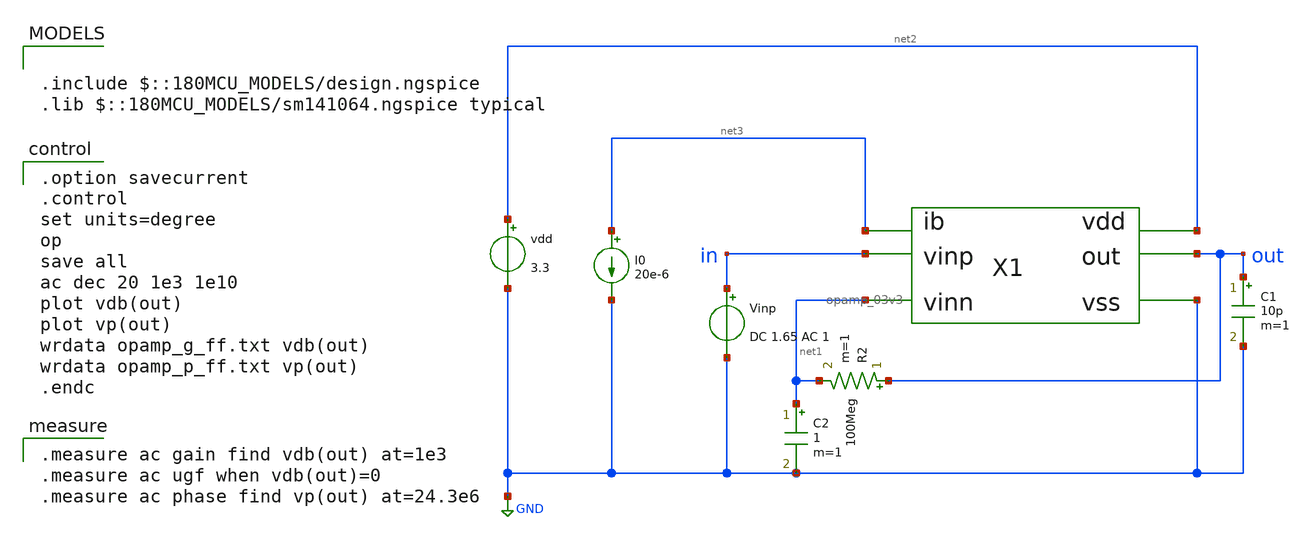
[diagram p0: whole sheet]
** sch_path: opamp_ac_03v3.sch
**.subckt opamp_ac_03v3
vdd net2 GND 3.3
I0 net3 GND 20e-6
Vinp in GND DC 1.65 AC 1
R2 out net1 100Meg m=1
C2 net1 GND 1 m=1
C1 out GND 10p m=1
X1 net1 in net3 GND out net2 opamp_03v3
**** begin user architecture code

.include $::180MCU_MODELS/design.ngspice
.lib $::180MCU_MODELS/sm141064.ngspice typical


.option savecurrent
.control
set units=degree
op
save all
ac dec 20 1e3 1e10
plot vdb(out)
plot vp(out)
wrdata opamp_g_ff.txt vdb(out)
wrdata opamp_p_ff.txt vp(out)
.endc


.measure ac gain find vdb(out) at=1e3
.measure ac ugf when vdb(out)=0
.measure ac phase find vp(out) at=24.3e6

**** end user architecture code
**.ends

* expanding   symbol:  opamp_03v3.sym # of pins=6
** sym_path: opamp_03v3.sym
** sch_path: opamp_03v3.sch
.subckt opamp_03v3 vinn vinp ib vss out vdd
*.iopin ib
*.iopin vdd
*.ipin vinn
*.opin out
*.iopin vss
*.ipin vinp
XM1 net4 vinn net3 net3 pfet_03v3 L=0.56u W=56u nf=1 ad='int((nf+1)/2) * W/nf * 0.18u' as='int((nf+2)/2) * W/nf * 0.18u'
+ pd='2*int((nf+1)/2) * (W/nf + 0.18u)' ps='2*int((nf+2)/2) * (W/nf + 0.18u)' nrd='0.18u / W' nrs='0.18u / W'
+ sa=0 sb=0 sd=0 m=1
XM2 net5 vinp net3 net3 pfet_03v3 L=0.56u W=56u nf=1 ad='int((nf+1)/2) * W/nf * 0.18u' as='int((nf+2)/2) * W/nf * 0.18u'
+ pd='2*int((nf+1)/2) * (W/nf + 0.18u)' ps='2*int((nf+2)/2) * (W/nf + 0.18u)' nrd='0.18u / W' nrs='0.18u / W'
+ sa=0 sb=0 sd=0 m=1
XM3 net4 net4 vss vss nfet_03v3 L=0.56u W=2.8u nf=1 ad='int((nf+1)/2) * W/nf * 0.18u' as='int((nf+2)/2) * W/nf * 0.18u'
+ pd='2*int((nf+1)/2) * (W/nf + 0.18u)' ps='2*int((nf+2)/2) * (W/nf + 0.18u)' nrd='0.18u / W' nrs='0.18u / W'
+ sa=0 sb=0 sd=0 m=1
XM4 net5 net4 vss vss nfet_03v3 L=0.56u W=2.8u nf=1 ad='int((nf+1)/2) * W/nf * 0.18u' as='int((nf+2)/2) * W/nf * 0.18u'
+ pd='2*int((nf+1)/2) * (W/nf + 0.18u)' ps='2*int((nf+2)/2) * (W/nf + 0.18u)' nrd='0.18u / W' nrs='0.18u / W'
+ sa=0 sb=0 sd=0 m=1
XM5 net3 ib vdd vdd pfet_03v3 L=0.56u W=11.2u nf=1 ad='int((nf+1)/2) * W/nf * 0.18u' as='int((nf+2)/2) * W/nf * 0.18u'
+ pd='2*int((nf+1)/2) * (W/nf + 0.18u)' ps='2*int((nf+2)/2) * (W/nf + 0.18u)' nrd='0.18u / W' nrs='0.18u / W'
+ sa=0 sb=0 sd=0 m=1
XM6 out ib vdd vdd pfet_03v3 L=0.56u W=56u nf=1 ad='int((nf+1)/2) * W/nf * 0.18u' as='int((nf+2)/2) * W/nf * 0.18u'
+ pd='2*int((nf+1)/2) * (W/nf + 0.18u)' ps='2*int((nf+2)/2) * (W/nf + 0.18u)' nrd='0.18u / W' nrs='0.18u / W'
+ sa=0 sb=0 sd=0 m=1
XM7 out net5 vss vss nfet_03v3 L=0.56u W=56u nf=1 ad='int((nf+1)/2) * W/nf * 0.18u' as='int((nf+2)/2) * W/nf * 0.18u'
+ pd='2*int((nf+1)/2) * (W/nf + 0.18u)' ps='2*int((nf+2)/2) * (W/nf + 0.18u)' nrd='0.18u / W' nrs='0.18u / W'
+ sa=0 sb=0 sd=0 m=1
C1 out net6 1p m=1
XM8 ib ib vdd vdd pfet_03v3 L=0.56u W=5.6u nf=1 ad='int((nf+1)/2) * W/nf * 0.18u' as='int((nf+2)/2) * W/nf * 0.18u'
+ pd='2*int((nf+1)/2) * (W/nf + 0.18u)' ps='2*int((nf+2)/2) * (W/nf + 0.18u)' nrd='0.18u / W' nrs='0.18u / W'
+ sa=0 sb=0 sd=0 m=1
XM9 net1 ib vdd vdd pfet_03v3 L=0.56u W=5.6u nf=1 ad='int((nf+1)/2) * W/nf * 0.18u' as='int((nf+2)/2) * W/nf * 0.18u'
+ pd='2*int((nf+1)/2) * (W/nf + 0.18u)' ps='2*int((nf+2)/2) * (W/nf + 0.18u)' nrd='0.18u / W' nrs='0.18u / W'
+ sa=0 sb=0 sd=0 m=1
XM10 net1 net1 net2 vss nfet_03v3 L=0.56u W=2.8u nf=1 ad='int((nf+1)/2) * W/nf * 0.18u' as='int((nf+2)/2) * W/nf * 0.18u'
+ pd='2*int((nf+1)/2) * (W/nf + 0.18u)' ps='2*int((nf+2)/2) * (W/nf + 0.18u)' nrd='0.18u / W' nrs='0.18u / W'
+ sa=0 sb=0 sd=0 m=1
XM11 net2 net2 vss vss nfet_03v3 L=0.56u W=2.8u nf=1 ad='int((nf+1)/2) * W/nf * 0.18u' as='int((nf+2)/2) * W/nf * 0.18u'
+ pd='2*int((nf+1)/2) * (W/nf + 0.18u)' ps='2*int((nf+2)/2) * (W/nf + 0.18u)' nrd='0.18u / W' nrs='0.18u / W'
+ sa=0 sb=0 sd=0 m=1
XM12 net6 net1 net5 vss nfet_03v3 L=0.56u W=11.2u nf=1 ad='int((nf+1)/2) * W/nf * 0.18u' as='int((nf+2)/2) * W/nf * 0.18u'
+ pd='2*int((nf+1)/2) * (W/nf + 0.18u)' ps='2*int((nf+2)/2) * (W/nf + 0.18u)' nrd='0.18u / W' nrs='0.18u / W'
+ sa=0 sb=0 sd=0 m=1
.ends

.GLOBAL GND
.end
